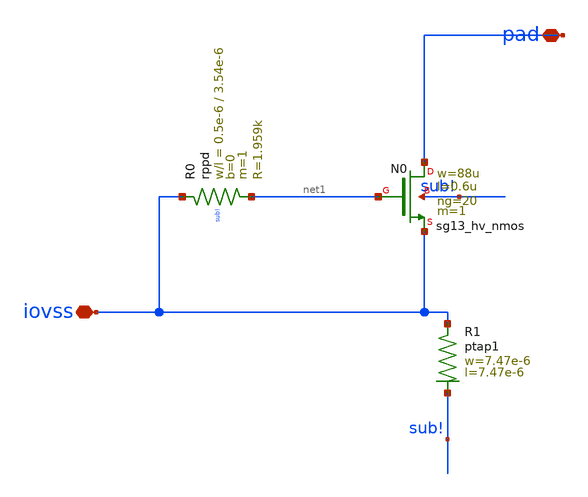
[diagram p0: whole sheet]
** sch_path: ihp-sg13g2/libs.ref/sg13g2_io/sch/xschem/sg13g2_Clamp_N20N0D.sch
**.subckt sg13g2_Clamp_N20N0D pad iovss
*.iopin pad
*.iopin iovss
XN0 pad net1 iovss sub! sg13_hv_nmos w=88u l=0.6u ng=20 m=1 mm_ok=1
XR0 iovss net1 sub! rppd w=0.5e-6 l=3.54e-6 m=1 b=0 mm_ok=1
XR1 iovss sub! ptap1 R=11.44 w=7.47e-6 l=7.47e-6
**.ends
.end
